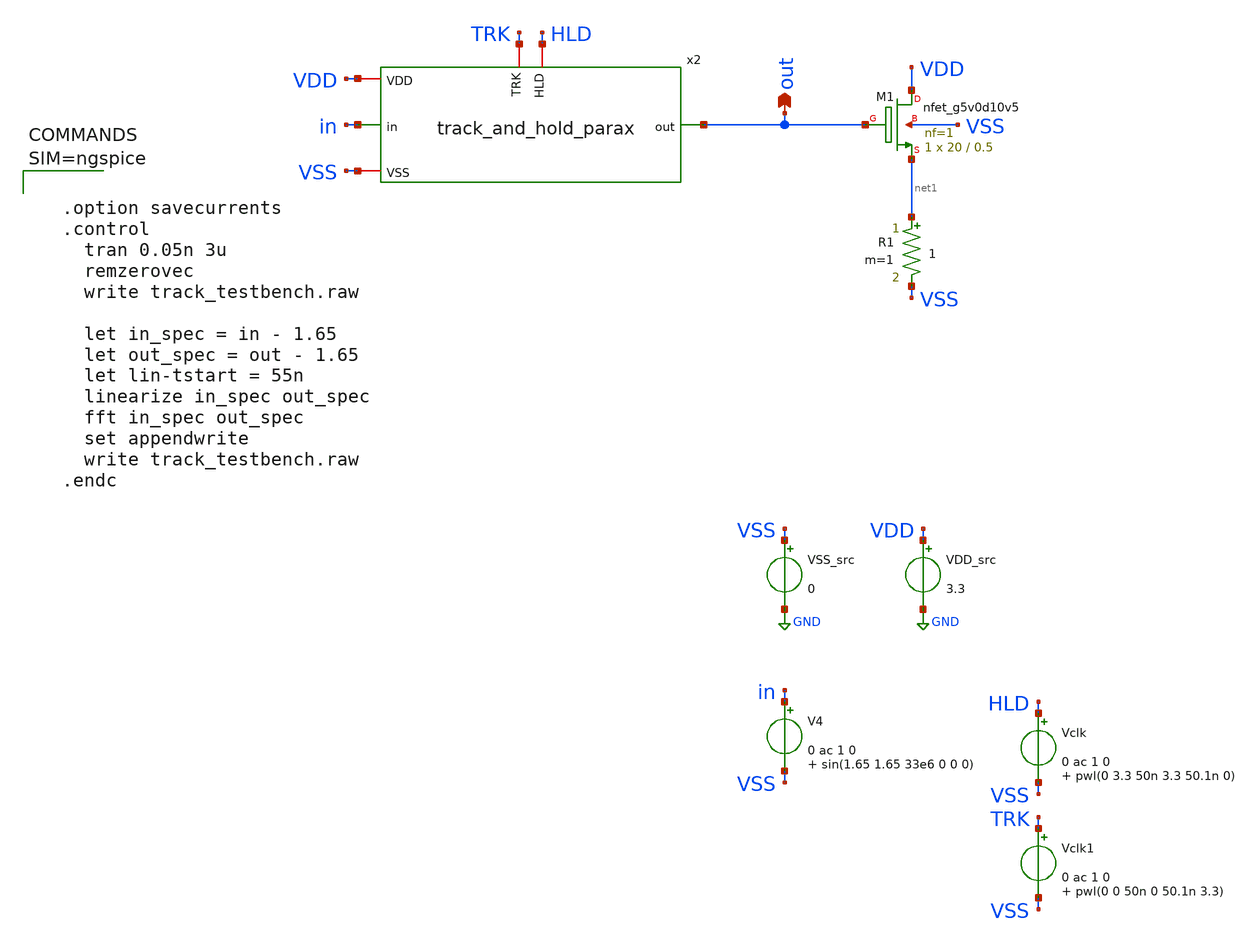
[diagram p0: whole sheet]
** sch_path: xschem/track_and_hold/track_testbench.sch
**.subckt track_testbench out
*.opin out
VDD_src VDD GND 3.3
VSS_src VSS GND 0
V4 in VSS 0 ac 1 0 sin(1.65 1.65 33e6 0 0 0)
XM1 VDD out net1 VSS sky130_fd_pr__nfet_g5v0d10v5 L=0.5 W=20 nf=1 ad='int((nf+1)/2) * W/nf * 0.29' as='int((nf+2)/2) * W/nf * 0.29'
+ pd='2*int((nf+1)/2) * (W/nf + 0.29)' ps='2*int((nf+2)/2) * (W/nf + 0.29)' nrd='0.29 / W' nrs='0.29 / W'
+ sa=0 sb=0 sd=0 mult=1 m=1
R1 net1 VSS 1 m=1
Vclk HLD VSS 0 ac 1 0 pwl(0 3.3 50n 3.3 50.1n 0)
Vclk1 TRK VSS 0 ac 1 0 pwl(0 0 50n 0 50.1n 3.3)
x2 HLD TRK VDD VSS out in track_and_hold_parax
**** begin user architecture code

** opencircuitdesign pdks install
.lib $::SKYWATER_MODELS/sky130.lib.spice tt





  .option savecurrents
  .control
    tran 0.05n 3u
    remzerovec
    write track_testbench.raw

    let in_spec = in - 1.65
    let out_spec = out - 1.65
    let lin-tstart = 55n
    linearize in_spec out_spec
    fft in_spec out_spec
    set appendwrite
    write track_testbench.raw
  .endc



**** end user architecture code
**.ends

* expanding   symbol:  track_and_hold_parax.sym # of pins=6
** sym_path: xschem/track_and_hold.sym
.include [file normalize ../../mag/track_and_hold.sim.spice]
.GLOBAL GND
.end
